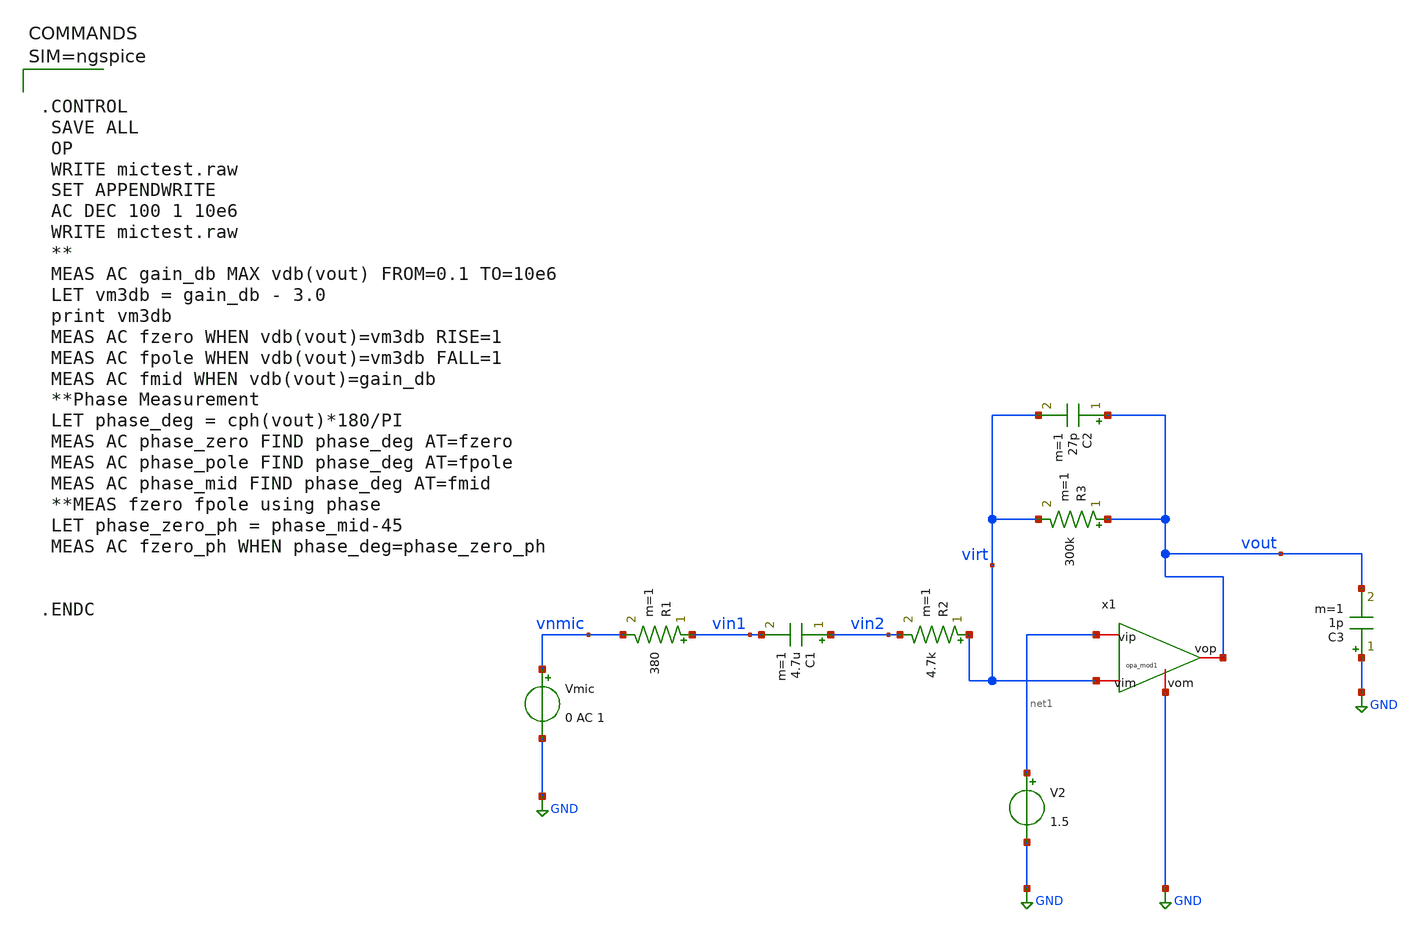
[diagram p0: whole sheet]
** sch_path: xschem/mictest_Opamp.sch
**.subckt mictest_Opamp
Vmic vnmic GND 0 AC 1
R1 vin1 vnmic 380 m=1
C1 vin2 vin1 4.7u m=1
R2 virt vin2 4.7k m=1
R3 vout virt 300k m=1
C2 vout virt 27p m=1
V2 net1 GND 1.5
C3 GND vout 1p m=1
x1 vout net1 virt GND opa_mod1
**** begin user architecture code



.CONTROL
 SAVE ALL
 OP
 WRITE mictest.raw
 SET APPENDWRITE
 AC DEC 100 1 10e6
 WRITE mictest.raw
 **
 MEAS AC gain_db MAX vdb(vout) FROM=0.1 TO=10e6
 LET vm3db = gain_db - 3.0
 print vm3db
 MEAS AC fzero WHEN vdb(vout)=vm3db RISE=1
 MEAS AC fpole WHEN vdb(vout)=vm3db FALL=1
 MEAS AC fmid WHEN vdb(vout)=gain_db
 **Phase Measurement
 LET phase_deg = cph(vout)*180/PI
 MEAS AC phase_zero FIND phase_deg AT=fzero
 MEAS AC phase_pole FIND phase_deg AT=fpole
 MEAS AC phase_mid FIND phase_deg AT=fmid
 **MEAS fzero fpole using phase
 LET phase_zero_ph = phase_mid-45
 MEAS AC fzero_ph WHEN phase_deg=phase_zero_ph


.ENDC



**** end user architecture code
**.ends
.GLOBAL GND
.end
